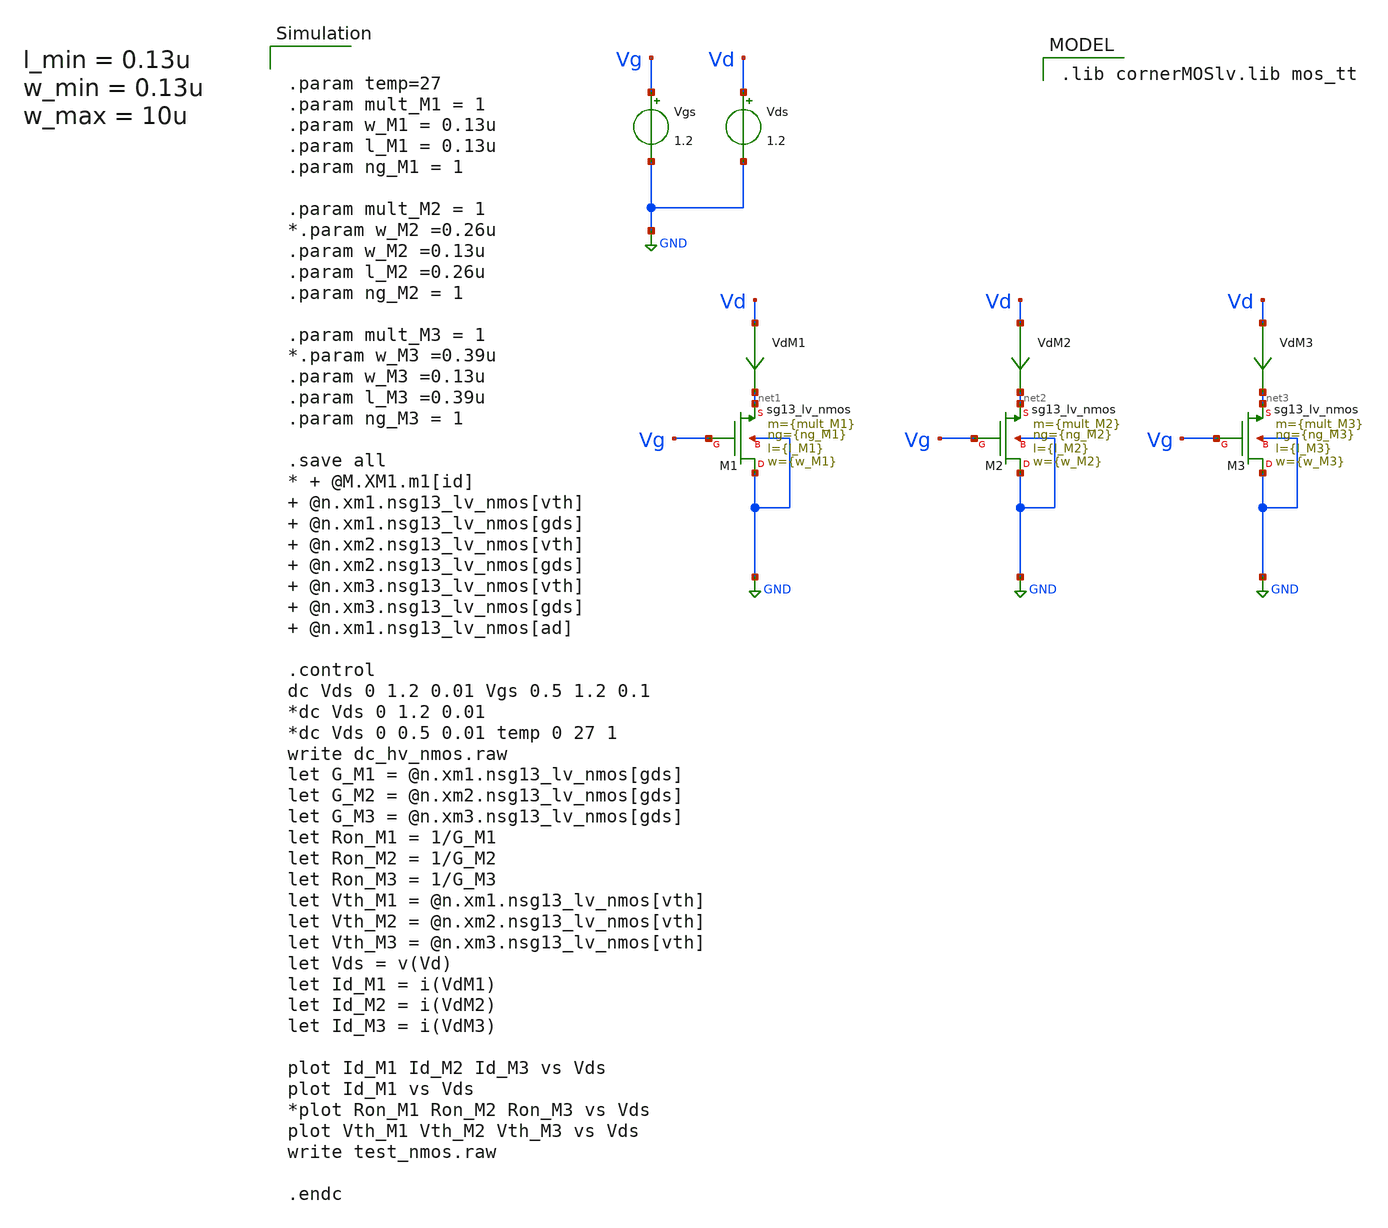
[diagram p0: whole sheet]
** sch_path: ChipUSM_AnalogTrack24/TestBenchs/TB_lvNMOS_charact.sch
**.subckt TB_lvNMOS_charact
XM1 GND Vg net1 GND sg13_lv_nmos w={w_M1} l={l_M1} ng={ng_M1} m={mult_M1} mm_ok=1
VdM1 Vd net1 0
.save i(vdm1)
VdM2 Vd net2 0
.save i(vdm2)
VdM3 Vd net3 0
.save i(vdm3)
Vgs Vg GND 1.2
Vds Vd GND 1.2
XM2 GND Vg net2 GND sg13_lv_nmos w={w_M2} l={l_M2} ng={ng_M2} m={mult_M2} mm_ok=1
XM3 GND Vg net3 GND sg13_lv_nmos w={w_M3} l={l_M3} ng={ng_M3} m={mult_M3} mm_ok=1
**** begin user architecture code


.param temp=27
.param mult_M1 = 1
.param w_M1 = 0.13u
.param l_M1 = 0.13u
.param ng_M1 = 1

.param mult_M2 = 1
*.param w_M2 =0.26u
.param w_M2 =0.13u
.param l_M2 =0.26u
.param ng_M2 = 1

.param mult_M3 = 1
*.param w_M3 =0.39u
.param w_M3 =0.13u
.param l_M3 =0.39u
.param ng_M3 = 1

.save all
* + @M.XM1.m1[id]  @n.xm1.nsg13_lv_nmos[vth]  @n.xm1.nsg13_lv_nmos[gds]  @n.xm2.nsg13_lv_nmos[vth]
*+  @n.xm2.nsg13_lv_nmos[gds]  @n.xm3.nsg13_lv_nmos[vth]  @n.xm3.nsg13_lv_nmos[gds]  @n.xm1.nsg13_lv_nmos[ad]

.control
dc Vds 0 1.2 0.01 Vgs 0.5 1.2 0.1
*dc Vds 0 1.2 0.01
*dc Vds 0 0.5 0.01 temp 0 27 1
write dc_hv_nmos.raw
let G_M1 = @n.xm1.nsg13_lv_nmos[gds]
let G_M2 = @n.xm2.nsg13_lv_nmos[gds]
let G_M3 = @n.xm3.nsg13_lv_nmos[gds]
let Ron_M1 = 1/G_M1
let Ron_M2 = 1/G_M2
let Ron_M3 = 1/G_M3
let Vth_M1 = @n.xm1.nsg13_lv_nmos[vth]
let Vth_M2 = @n.xm2.nsg13_lv_nmos[vth]
let Vth_M3 = @n.xm3.nsg13_lv_nmos[vth]
let Vds = v(Vd)
let Id_M1 = i(VdM1)
let Id_M2 = i(VdM2)
let Id_M3 = i(VdM3)

plot Id_M1 Id_M2 Id_M3 vs Vds
plot Id_M1 vs Vds
*plot Ron_M1 Ron_M2 Ron_M3 vs Vds
plot Vth_M1 Vth_M2 Vth_M3 vs Vds
write test_nmos.raw

.endc


 .lib cornerMOSlv.lib mos_tt

**** end user architecture code
**.ends
.GLOBAL GND
.end
